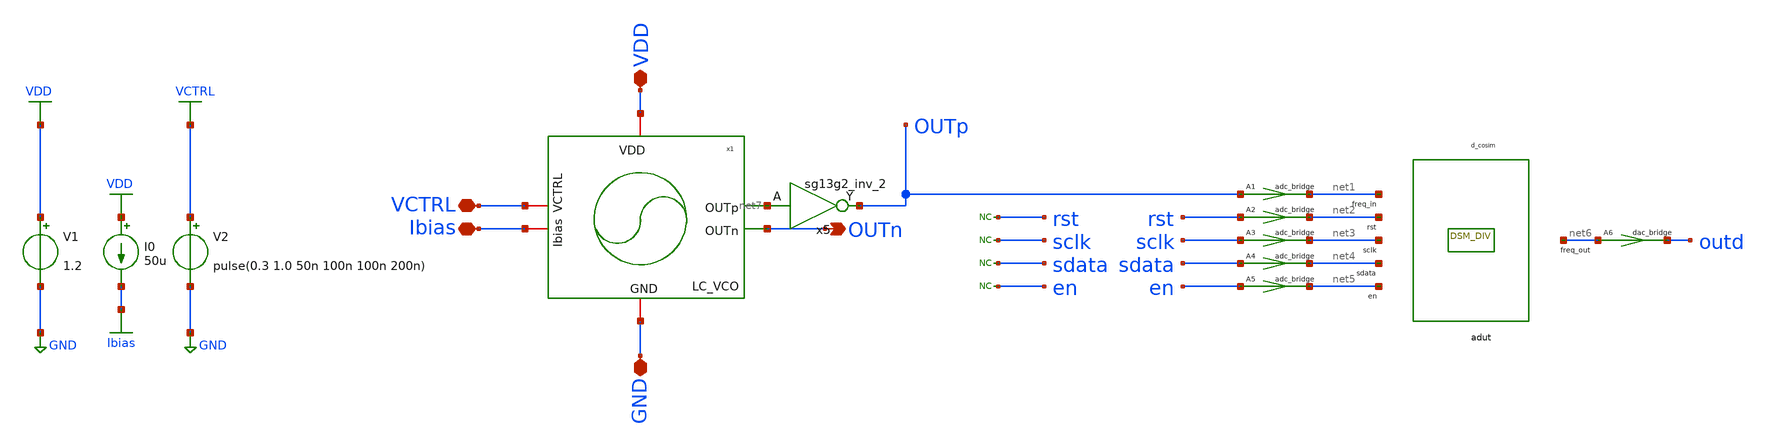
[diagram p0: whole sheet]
** sch_path: schematic/blocks/top-pll/LCVCO_DSM_tb.sch
* IHP-GmbH/IHP-Open-PDK/ihp-sg13g2/libs.tech/xschem/sg13g2_stdcells/sg13g2_inv_2.sch:
* Copyright 2023 IHP PDK Authors
* Licensed under the Apache License, Version 2.0 (the "License");
**.subckt LCVCO_DSM_tb OUTn VDD VCTRL GND Ibias
*.opin OUTn
*.iopin VDD
*.iopin VCTRL
*.iopin GND
*.iopin Ibias
* noconn rst
* noconn sclk
* noconn sdata
* noconn en
A1 [ OUTp ] [ net1 ] adc1
.model adc1 adc_bridge in_low=0.4 in_high=0.6
A2 [ rst ] [ net2 ] adc1
.model adc1 adc_bridge in_low=0.4 in_high=0.6
A3 [ sclk ] [ net3 ] adc1
.model adc1 adc_bridge in_low=0.4 in_high=0.6
A4 [ sdata ] [ net4 ] adc1
.model adc1 adc_bridge in_low=0.4 in_high=0.6
A5 [ en ] [ net5 ] adc1
.model adc1 adc_bridge in_low=0.4 in_high=0.6
adut [ net1 net2 net3 net4 net5 ] [ net6 ] null dut
.model dut d_cosim simulation=./../dsm_and_freq_divider.so
A6 [ net6 ] [ outd ] dac1
.model dac1 dac_bridge out_low=0 out_high=1.2
V1 VDD GND 1.2
V2 VCTRL GND pulse(0.3 1.0 50n 100n 100n 200n)
I0 VDD Ibias 50u
x5 OUTp net7 VDD GND sg13g2_inv_2
x1 VDD net7 OUTn Ibias VCTRL GND LC_VCO
**** begin user architecture code



.lib $::SG13G2_MODELS/cornerMOSlv.lib mos_tt
.lib $::SG13G2_MODELS/cornerMOShv.lib mos_tt
.lib $::SG13G2_MODELS/cornerHBT.lib hbt_typ
.lib $::SG13G2_MODELS/cornerRES.lib res_typ
.lib $::SG13G2_MODELS/cornerDIO.lib dio_tt
.lib $::SG13G2_MODELS/cornerCAP.lib cap_typ
.include /home/mmhnbm/.ciel/ciel/ihp-sg13g2/versions/c4b8b4e5e7a05f375cca3815d51b3a37721fbf5c/ihp-sg13g2/libs.ref/sg13g2_stdcell/spice/sg13g2_stdcell.spice
.global VDD GND






.include ./IHP_4nH_Inductor.spice
.param temp=27
.control
save V(VCTRL) V(OUTp) V(outd) V(sdata) V(sclk) V(en) V(rst)
.options maxstep=50p reltol=1e-3 abstol=1e-6

*.ic v(OUTp)=0.6
tran 1p 400n
remzerovec

* Save transient waveform to raw file
write LCVCO_DSM.raw

*quit 0
.endc


* to generate following file copy stimuli.test
* to the simulation directory and run simulation -> Utile Stimuli Editor (GUI),
* and press 'Translate'
.include stimuli_test.cir



**** end user architecture code
**.ends

* expanding   symbol:  sg13g2_stdcells/sg13g2_inv_2.sym # of pins=2
** sym_path: sg13g2_stdcells/sg13g2_inv_2.sym
** sch_path: sg13g2_stdcells/sg13g2_inv_2.sch
.subckt sg13g2_inv_2 Y A VDD VSS
*.opin Y
*.ipin A
*.iopin VDD
*.iopin VSS
XM1 Y A VSS VSS sg13_lv_nmos w=1.48u l=130.00n ng=2 m=1 mm_ok=1
XM2 Y A VDD VDD sg13_lv_pmos w=2.24u l=130.00n ng=2 m=1 mm_ok=1
.ends


* expanding   symbol:  /home/mmhnbm/frac-n-pll-vco-smacd_2026/schematic/blocks/lc-vco/LC_VCO.sym #
*+ of pins=6
** sym_path: /home/mmhnbm/frac-n-pll-vco-smacd_2026/schematic/blocks/lc-vco/LC_VCO.sym
** sch_path: /home/mmhnbm/frac-n-pll-vco-smacd_2026/schematic/blocks/lc-vco/LC_VCO.sch
.subckt LC_VCO VDD OUTp OUTn Ibias VCTRL GND
*.iopin VDD
*.opin OUTp
*.opin OUTn
*.iopin GND
*.iopin VCTRL
*.iopin Ibias
XM6 net1 Ibias GND GND sg13_lv_nmos w=1u l=0.15u ng=1 m=60 mm_ok=1
XM5 Ibias Ibias GND GND sg13_lv_nmos w=1u l=0.15u ng=1 m=1 mm_ok=1
XM4 OUTp OUTn VDD VDD sg13_lv_pmos w=8.5u l=0.5u ng=1 m=13 mm_ok=1
X5M3 OUTn OUTp VDD VDD sg13_lv_pmos w=8.5u l=0.5u ng=1 m=13 mm_ok=1
XM2 OUTp OUTn net1 GND sg13_lv_nmos w=2u l=0.5u ng=1 m=12 mm_ok=1
XM1 OUTn OUTp net1 GND sg13_lv_nmos w=2u l=0.5u ng=1 m=12 mm_ok=1
XC3 OUTp OUTn cap_cmim w=4.0e-6 l=4.0e-6 m=13.6 mm_ok=1
XMv2 OUTp VCTRL OUTp VDD sg13_lv_pmos w=4u l=4u ng=1 m=22 mm_ok=1
XMv1 OUTn VCTRL OUTn VDD sg13_lv_pmos w=4u l=4u ng=1 m=22 mm_ok=1
XR1 OUTp OUTn sub! rhigh w=1e-6 l=1e-6 m=1.23 b=0 mm_ok=1
x1 OUTn OUTp ihp_4nh_inductor
.ends

.GLOBAL GND
.GLOBAL VDD
.GLOBAL VCTRL
.GLOBAL Ibias
.end
